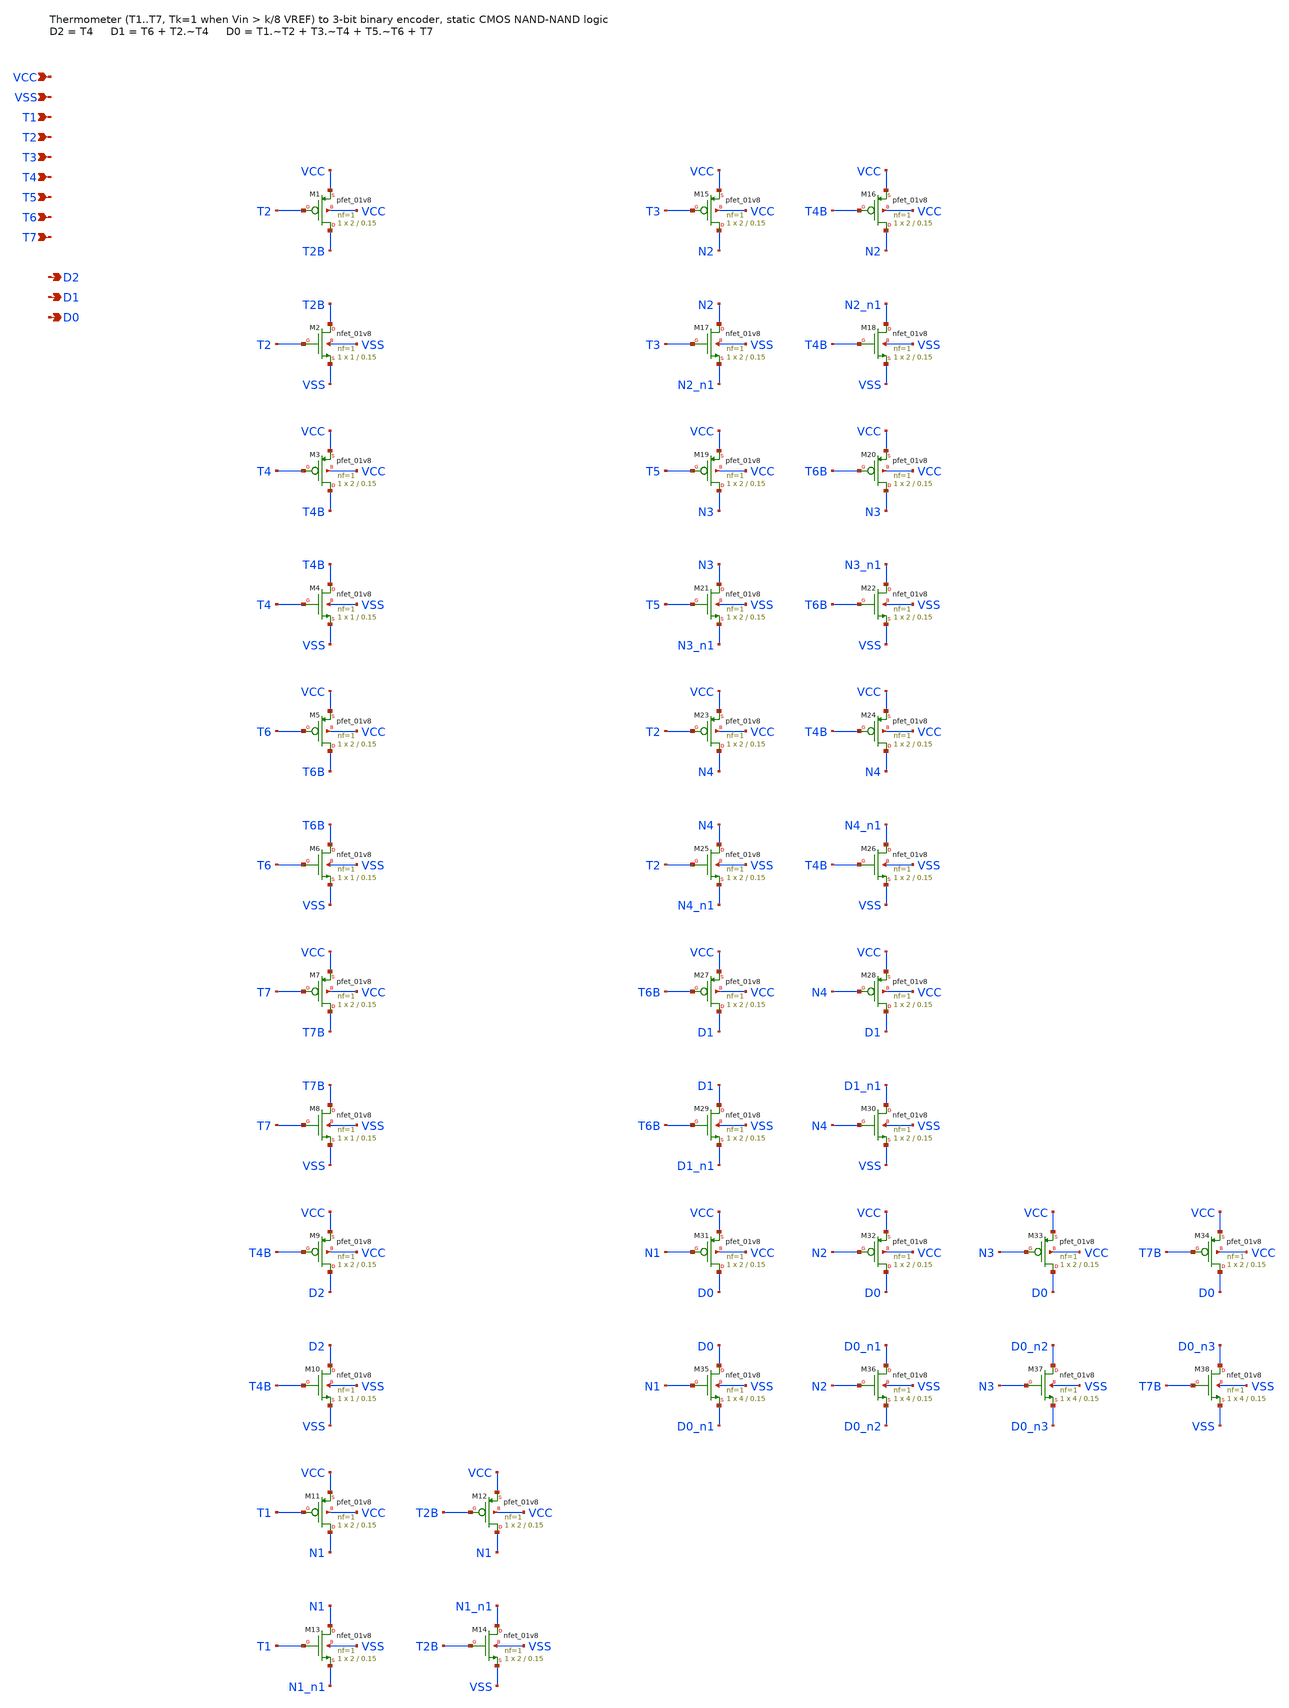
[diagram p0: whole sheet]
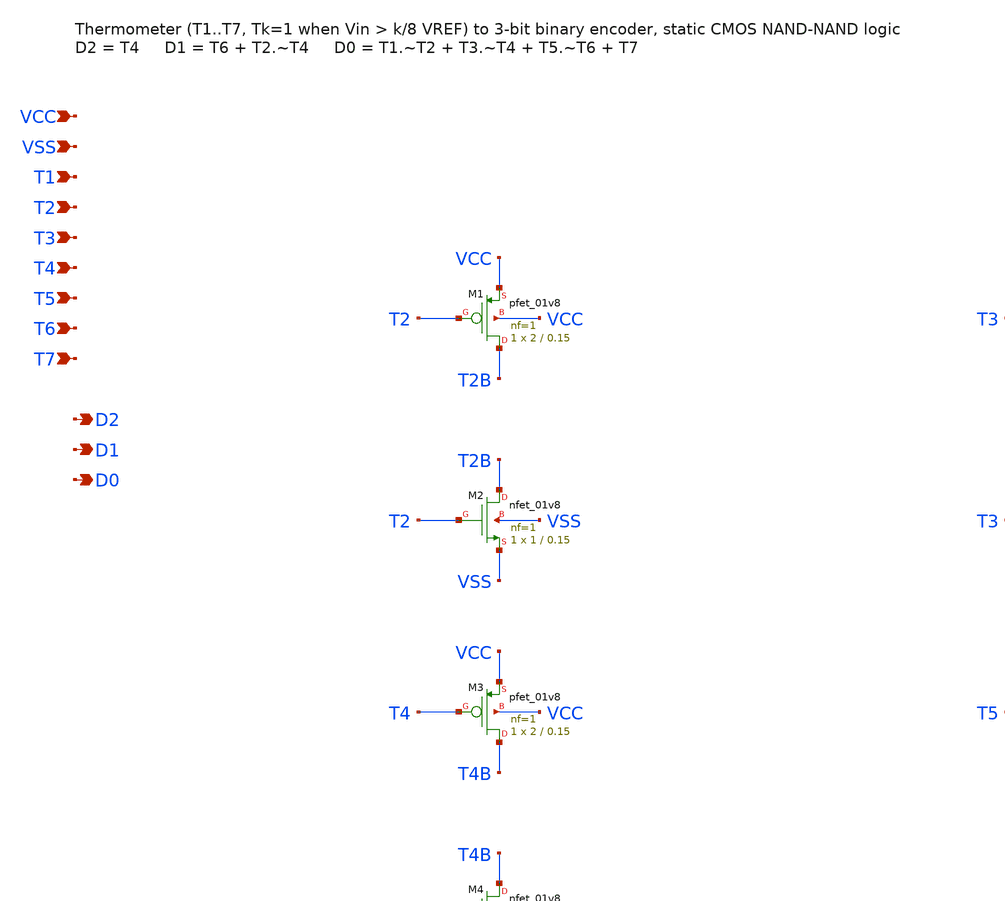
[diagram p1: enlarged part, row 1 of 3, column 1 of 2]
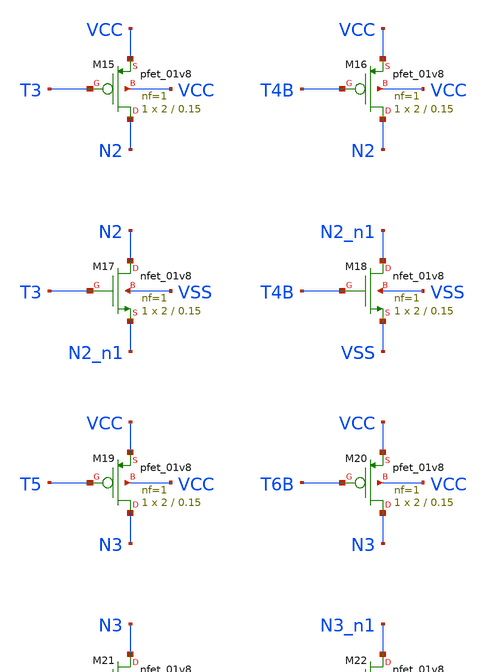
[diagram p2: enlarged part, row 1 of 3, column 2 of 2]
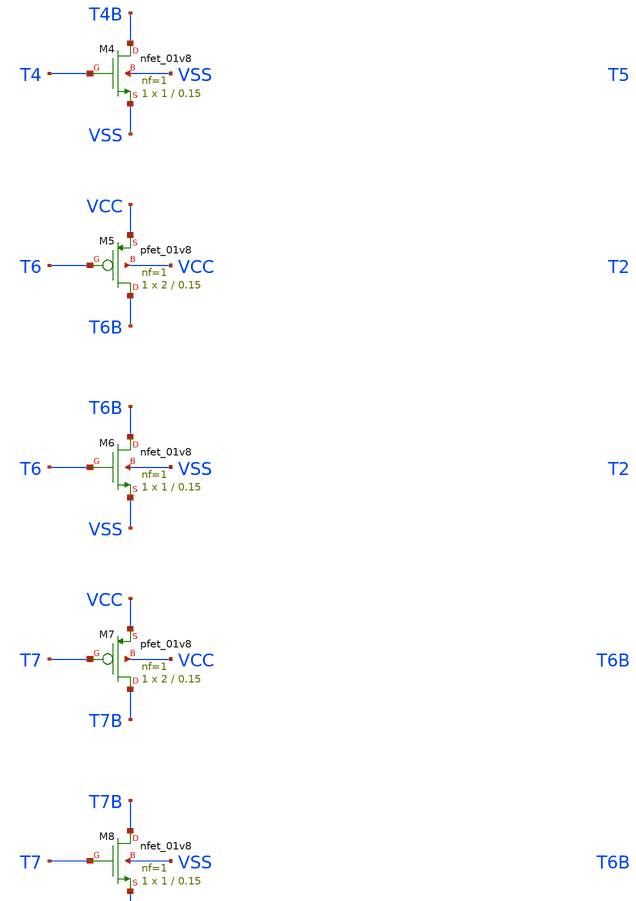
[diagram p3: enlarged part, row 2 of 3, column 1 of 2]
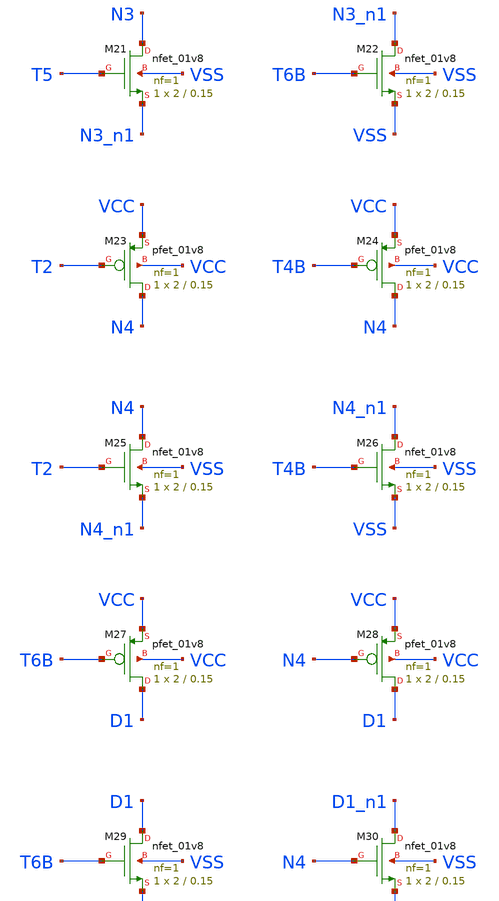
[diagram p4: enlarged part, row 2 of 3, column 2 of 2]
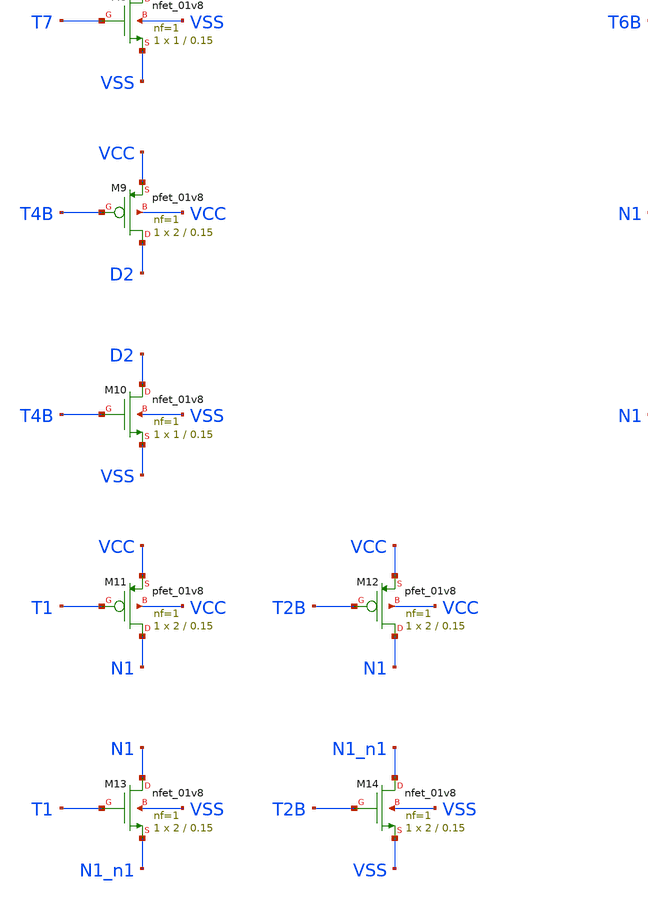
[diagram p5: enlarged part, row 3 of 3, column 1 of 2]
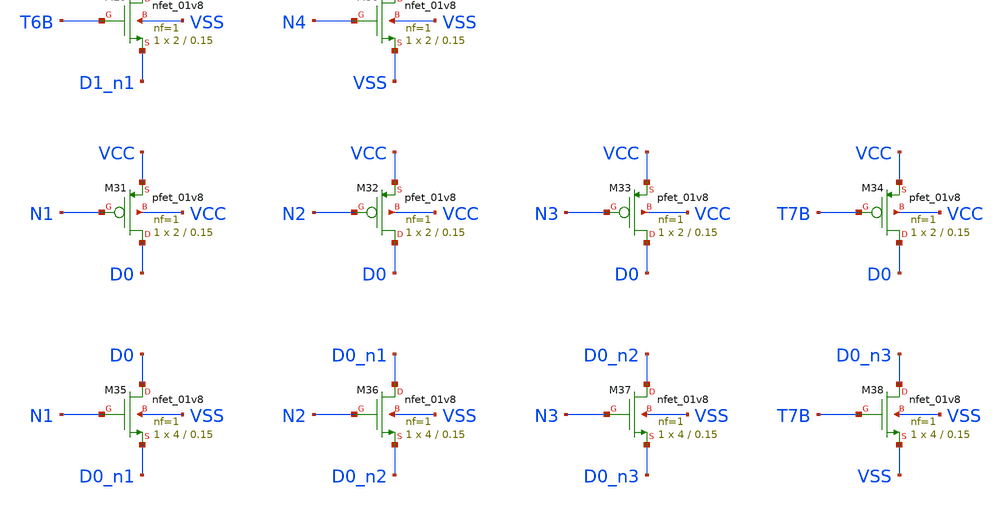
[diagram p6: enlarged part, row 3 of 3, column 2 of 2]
** sch_path: therm2bin3.sch
**.subckt therm2bin3 VCC VSS T1 T2 T3 T4 T5 T6 T7 D2 D1 D0
*.ipin VCC
*.ipin VSS
*.ipin T1
*.ipin T2
*.ipin T3
*.ipin T4
*.ipin T5
*.ipin T6
*.ipin T7
*.opin D2
*.opin D1
*.opin D0
XM1 T2B T2 VCC VCC sky130_fd_pr__pfet_01v8 L=0.15 W=2 nf=1 ad='int((nf+1)/2) * W/nf * 0.29' as='int((nf+2)/2) * W/nf * 0.29'
+ pd='2*int((nf+1)/2) * (W/nf + 0.29)' ps='2*int((nf+2)/2) * (W/nf + 0.29)' nrd='0.29 / W' nrs='0.29 / W'
+ sa=0 sb=0 sd=0 mult=1 m=1
XM2 T2B T2 VSS VSS sky130_fd_pr__nfet_01v8 L=0.15 W=1 nf=1 ad='int((nf+1)/2) * W/nf * 0.29' as='int((nf+2)/2) * W/nf * 0.29'
+ pd='2*int((nf+1)/2) * (W/nf + 0.29)' ps='2*int((nf+2)/2) * (W/nf + 0.29)' nrd='0.29 / W' nrs='0.29 / W'
+ sa=0 sb=0 sd=0 mult=1 m=1
XM3 T4B T4 VCC VCC sky130_fd_pr__pfet_01v8 L=0.15 W=2 nf=1 ad='int((nf+1)/2) * W/nf * 0.29' as='int((nf+2)/2) * W/nf * 0.29'
+ pd='2*int((nf+1)/2) * (W/nf + 0.29)' ps='2*int((nf+2)/2) * (W/nf + 0.29)' nrd='0.29 / W' nrs='0.29 / W'
+ sa=0 sb=0 sd=0 mult=1 m=1
XM4 T4B T4 VSS VSS sky130_fd_pr__nfet_01v8 L=0.15 W=1 nf=1 ad='int((nf+1)/2) * W/nf * 0.29' as='int((nf+2)/2) * W/nf * 0.29'
+ pd='2*int((nf+1)/2) * (W/nf + 0.29)' ps='2*int((nf+2)/2) * (W/nf + 0.29)' nrd='0.29 / W' nrs='0.29 / W'
+ sa=0 sb=0 sd=0 mult=1 m=1
XM5 T6B T6 VCC VCC sky130_fd_pr__pfet_01v8 L=0.15 W=2 nf=1 ad='int((nf+1)/2) * W/nf * 0.29' as='int((nf+2)/2) * W/nf * 0.29'
+ pd='2*int((nf+1)/2) * (W/nf + 0.29)' ps='2*int((nf+2)/2) * (W/nf + 0.29)' nrd='0.29 / W' nrs='0.29 / W'
+ sa=0 sb=0 sd=0 mult=1 m=1
XM6 T6B T6 VSS VSS sky130_fd_pr__nfet_01v8 L=0.15 W=1 nf=1 ad='int((nf+1)/2) * W/nf * 0.29' as='int((nf+2)/2) * W/nf * 0.29'
+ pd='2*int((nf+1)/2) * (W/nf + 0.29)' ps='2*int((nf+2)/2) * (W/nf + 0.29)' nrd='0.29 / W' nrs='0.29 / W'
+ sa=0 sb=0 sd=0 mult=1 m=1
XM7 T7B T7 VCC VCC sky130_fd_pr__pfet_01v8 L=0.15 W=2 nf=1 ad='int((nf+1)/2) * W/nf * 0.29' as='int((nf+2)/2) * W/nf * 0.29'
+ pd='2*int((nf+1)/2) * (W/nf + 0.29)' ps='2*int((nf+2)/2) * (W/nf + 0.29)' nrd='0.29 / W' nrs='0.29 / W'
+ sa=0 sb=0 sd=0 mult=1 m=1
XM8 T7B T7 VSS VSS sky130_fd_pr__nfet_01v8 L=0.15 W=1 nf=1 ad='int((nf+1)/2) * W/nf * 0.29' as='int((nf+2)/2) * W/nf * 0.29'
+ pd='2*int((nf+1)/2) * (W/nf + 0.29)' ps='2*int((nf+2)/2) * (W/nf + 0.29)' nrd='0.29 / W' nrs='0.29 / W'
+ sa=0 sb=0 sd=0 mult=1 m=1
XM9 D2 T4B VCC VCC sky130_fd_pr__pfet_01v8 L=0.15 W=2 nf=1 ad='int((nf+1)/2) * W/nf * 0.29' as='int((nf+2)/2) * W/nf * 0.29'
+ pd='2*int((nf+1)/2) * (W/nf + 0.29)' ps='2*int((nf+2)/2) * (W/nf + 0.29)' nrd='0.29 / W' nrs='0.29 / W'
+ sa=0 sb=0 sd=0 mult=1 m=1
XM10 D2 T4B VSS VSS sky130_fd_pr__nfet_01v8 L=0.15 W=1 nf=1 ad='int((nf+1)/2) * W/nf * 0.29' as='int((nf+2)/2) * W/nf * 0.29'
+ pd='2*int((nf+1)/2) * (W/nf + 0.29)' ps='2*int((nf+2)/2) * (W/nf + 0.29)' nrd='0.29 / W' nrs='0.29 / W'
+ sa=0 sb=0 sd=0 mult=1 m=1
XM11 N1 T1 VCC VCC sky130_fd_pr__pfet_01v8 L=0.15 W=2 nf=1 ad='int((nf+1)/2) * W/nf * 0.29' as='int((nf+2)/2) * W/nf * 0.29'
+ pd='2*int((nf+1)/2) * (W/nf + 0.29)' ps='2*int((nf+2)/2) * (W/nf + 0.29)' nrd='0.29 / W' nrs='0.29 / W'
+ sa=0 sb=0 sd=0 mult=1 m=1
XM12 N1 T2B VCC VCC sky130_fd_pr__pfet_01v8 L=0.15 W=2 nf=1 ad='int((nf+1)/2) * W/nf * 0.29' as='int((nf+2)/2) * W/nf * 0.29'
+ pd='2*int((nf+1)/2) * (W/nf + 0.29)' ps='2*int((nf+2)/2) * (W/nf + 0.29)' nrd='0.29 / W' nrs='0.29 / W'
+ sa=0 sb=0 sd=0 mult=1 m=1
XM13 N1 T1 N1_n1 VSS sky130_fd_pr__nfet_01v8 L=0.15 W=2 nf=1 ad='int((nf+1)/2) * W/nf * 0.29' as='int((nf+2)/2) * W/nf * 0.29'
+ pd='2*int((nf+1)/2) * (W/nf + 0.29)' ps='2*int((nf+2)/2) * (W/nf + 0.29)' nrd='0.29 / W' nrs='0.29 / W'
+ sa=0 sb=0 sd=0 mult=1 m=1
XM14 N1_n1 T2B VSS VSS sky130_fd_pr__nfet_01v8 L=0.15 W=2 nf=1 ad='int((nf+1)/2) * W/nf * 0.29' as='int((nf+2)/2) * W/nf * 0.29'
+ pd='2*int((nf+1)/2) * (W/nf + 0.29)' ps='2*int((nf+2)/2) * (W/nf + 0.29)' nrd='0.29 / W' nrs='0.29 / W'
+ sa=0 sb=0 sd=0 mult=1 m=1
XM15 N2 T3 VCC VCC sky130_fd_pr__pfet_01v8 L=0.15 W=2 nf=1 ad='int((nf+1)/2) * W/nf * 0.29' as='int((nf+2)/2) * W/nf * 0.29'
+ pd='2*int((nf+1)/2) * (W/nf + 0.29)' ps='2*int((nf+2)/2) * (W/nf + 0.29)' nrd='0.29 / W' nrs='0.29 / W'
+ sa=0 sb=0 sd=0 mult=1 m=1
XM16 N2 T4B VCC VCC sky130_fd_pr__pfet_01v8 L=0.15 W=2 nf=1 ad='int((nf+1)/2) * W/nf * 0.29' as='int((nf+2)/2) * W/nf * 0.29'
+ pd='2*int((nf+1)/2) * (W/nf + 0.29)' ps='2*int((nf+2)/2) * (W/nf + 0.29)' nrd='0.29 / W' nrs='0.29 / W'
+ sa=0 sb=0 sd=0 mult=1 m=1
XM17 N2 T3 N2_n1 VSS sky130_fd_pr__nfet_01v8 L=0.15 W=2 nf=1 ad='int((nf+1)/2) * W/nf * 0.29' as='int((nf+2)/2) * W/nf * 0.29'
+ pd='2*int((nf+1)/2) * (W/nf + 0.29)' ps='2*int((nf+2)/2) * (W/nf + 0.29)' nrd='0.29 / W' nrs='0.29 / W'
+ sa=0 sb=0 sd=0 mult=1 m=1
XM18 N2_n1 T4B VSS VSS sky130_fd_pr__nfet_01v8 L=0.15 W=2 nf=1 ad='int((nf+1)/2) * W/nf * 0.29' as='int((nf+2)/2) * W/nf * 0.29'
+ pd='2*int((nf+1)/2) * (W/nf + 0.29)' ps='2*int((nf+2)/2) * (W/nf + 0.29)' nrd='0.29 / W' nrs='0.29 / W'
+ sa=0 sb=0 sd=0 mult=1 m=1
XM19 N3 T5 VCC VCC sky130_fd_pr__pfet_01v8 L=0.15 W=2 nf=1 ad='int((nf+1)/2) * W/nf * 0.29' as='int((nf+2)/2) * W/nf * 0.29'
+ pd='2*int((nf+1)/2) * (W/nf + 0.29)' ps='2*int((nf+2)/2) * (W/nf + 0.29)' nrd='0.29 / W' nrs='0.29 / W'
+ sa=0 sb=0 sd=0 mult=1 m=1
XM20 N3 T6B VCC VCC sky130_fd_pr__pfet_01v8 L=0.15 W=2 nf=1 ad='int((nf+1)/2) * W/nf * 0.29' as='int((nf+2)/2) * W/nf * 0.29'
+ pd='2*int((nf+1)/2) * (W/nf + 0.29)' ps='2*int((nf+2)/2) * (W/nf + 0.29)' nrd='0.29 / W' nrs='0.29 / W'
+ sa=0 sb=0 sd=0 mult=1 m=1
XM21 N3 T5 N3_n1 VSS sky130_fd_pr__nfet_01v8 L=0.15 W=2 nf=1 ad='int((nf+1)/2) * W/nf * 0.29' as='int((nf+2)/2) * W/nf * 0.29'
+ pd='2*int((nf+1)/2) * (W/nf + 0.29)' ps='2*int((nf+2)/2) * (W/nf + 0.29)' nrd='0.29 / W' nrs='0.29 / W'
+ sa=0 sb=0 sd=0 mult=1 m=1
XM22 N3_n1 T6B VSS VSS sky130_fd_pr__nfet_01v8 L=0.15 W=2 nf=1 ad='int((nf+1)/2) * W/nf * 0.29' as='int((nf+2)/2) * W/nf * 0.29'
+ pd='2*int((nf+1)/2) * (W/nf + 0.29)' ps='2*int((nf+2)/2) * (W/nf + 0.29)' nrd='0.29 / W' nrs='0.29 / W'
+ sa=0 sb=0 sd=0 mult=1 m=1
XM23 N4 T2 VCC VCC sky130_fd_pr__pfet_01v8 L=0.15 W=2 nf=1 ad='int((nf+1)/2) * W/nf * 0.29' as='int((nf+2)/2) * W/nf * 0.29'
+ pd='2*int((nf+1)/2) * (W/nf + 0.29)' ps='2*int((nf+2)/2) * (W/nf + 0.29)' nrd='0.29 / W' nrs='0.29 / W'
+ sa=0 sb=0 sd=0 mult=1 m=1
XM24 N4 T4B VCC VCC sky130_fd_pr__pfet_01v8 L=0.15 W=2 nf=1 ad='int((nf+1)/2) * W/nf * 0.29' as='int((nf+2)/2) * W/nf * 0.29'
+ pd='2*int((nf+1)/2) * (W/nf + 0.29)' ps='2*int((nf+2)/2) * (W/nf + 0.29)' nrd='0.29 / W' nrs='0.29 / W'
+ sa=0 sb=0 sd=0 mult=1 m=1
XM25 N4 T2 N4_n1 VSS sky130_fd_pr__nfet_01v8 L=0.15 W=2 nf=1 ad='int((nf+1)/2) * W/nf * 0.29' as='int((nf+2)/2) * W/nf * 0.29'
+ pd='2*int((nf+1)/2) * (W/nf + 0.29)' ps='2*int((nf+2)/2) * (W/nf + 0.29)' nrd='0.29 / W' nrs='0.29 / W'
+ sa=0 sb=0 sd=0 mult=1 m=1
XM26 N4_n1 T4B VSS VSS sky130_fd_pr__nfet_01v8 L=0.15 W=2 nf=1 ad='int((nf+1)/2) * W/nf * 0.29' as='int((nf+2)/2) * W/nf * 0.29'
+ pd='2*int((nf+1)/2) * (W/nf + 0.29)' ps='2*int((nf+2)/2) * (W/nf + 0.29)' nrd='0.29 / W' nrs='0.29 / W'
+ sa=0 sb=0 sd=0 mult=1 m=1
XM27 D1 T6B VCC VCC sky130_fd_pr__pfet_01v8 L=0.15 W=2 nf=1 ad='int((nf+1)/2) * W/nf * 0.29' as='int((nf+2)/2) * W/nf * 0.29'
+ pd='2*int((nf+1)/2) * (W/nf + 0.29)' ps='2*int((nf+2)/2) * (W/nf + 0.29)' nrd='0.29 / W' nrs='0.29 / W'
+ sa=0 sb=0 sd=0 mult=1 m=1
XM28 D1 N4 VCC VCC sky130_fd_pr__pfet_01v8 L=0.15 W=2 nf=1 ad='int((nf+1)/2) * W/nf * 0.29' as='int((nf+2)/2) * W/nf * 0.29'
+ pd='2*int((nf+1)/2) * (W/nf + 0.29)' ps='2*int((nf+2)/2) * (W/nf + 0.29)' nrd='0.29 / W' nrs='0.29 / W'
+ sa=0 sb=0 sd=0 mult=1 m=1
XM29 D1 T6B D1_n1 VSS sky130_fd_pr__nfet_01v8 L=0.15 W=2 nf=1 ad='int((nf+1)/2) * W/nf * 0.29' as='int((nf+2)/2) * W/nf * 0.29'
+ pd='2*int((nf+1)/2) * (W/nf + 0.29)' ps='2*int((nf+2)/2) * (W/nf + 0.29)' nrd='0.29 / W' nrs='0.29 / W'
+ sa=0 sb=0 sd=0 mult=1 m=1
XM30 D1_n1 N4 VSS VSS sky130_fd_pr__nfet_01v8 L=0.15 W=2 nf=1 ad='int((nf+1)/2) * W/nf * 0.29' as='int((nf+2)/2) * W/nf * 0.29'
+ pd='2*int((nf+1)/2) * (W/nf + 0.29)' ps='2*int((nf+2)/2) * (W/nf + 0.29)' nrd='0.29 / W' nrs='0.29 / W'
+ sa=0 sb=0 sd=0 mult=1 m=1
XM31 D0 N1 VCC VCC sky130_fd_pr__pfet_01v8 L=0.15 W=2 nf=1 ad='int((nf+1)/2) * W/nf * 0.29' as='int((nf+2)/2) * W/nf * 0.29'
+ pd='2*int((nf+1)/2) * (W/nf + 0.29)' ps='2*int((nf+2)/2) * (W/nf + 0.29)' nrd='0.29 / W' nrs='0.29 / W'
+ sa=0 sb=0 sd=0 mult=1 m=1
XM32 D0 N2 VCC VCC sky130_fd_pr__pfet_01v8 L=0.15 W=2 nf=1 ad='int((nf+1)/2) * W/nf * 0.29' as='int((nf+2)/2) * W/nf * 0.29'
+ pd='2*int((nf+1)/2) * (W/nf + 0.29)' ps='2*int((nf+2)/2) * (W/nf + 0.29)' nrd='0.29 / W' nrs='0.29 / W'
+ sa=0 sb=0 sd=0 mult=1 m=1
XM33 D0 N3 VCC VCC sky130_fd_pr__pfet_01v8 L=0.15 W=2 nf=1 ad='int((nf+1)/2) * W/nf * 0.29' as='int((nf+2)/2) * W/nf * 0.29'
+ pd='2*int((nf+1)/2) * (W/nf + 0.29)' ps='2*int((nf+2)/2) * (W/nf + 0.29)' nrd='0.29 / W' nrs='0.29 / W'
+ sa=0 sb=0 sd=0 mult=1 m=1
XM34 D0 T7B VCC VCC sky130_fd_pr__pfet_01v8 L=0.15 W=2 nf=1 ad='int((nf+1)/2) * W/nf * 0.29' as='int((nf+2)/2) * W/nf * 0.29'
+ pd='2*int((nf+1)/2) * (W/nf + 0.29)' ps='2*int((nf+2)/2) * (W/nf + 0.29)' nrd='0.29 / W' nrs='0.29 / W'
+ sa=0 sb=0 sd=0 mult=1 m=1
XM35 D0 N1 D0_n1 VSS sky130_fd_pr__nfet_01v8 L=0.15 W=4 nf=1 ad='int((nf+1)/2) * W/nf * 0.29' as='int((nf+2)/2) * W/nf * 0.29'
+ pd='2*int((nf+1)/2) * (W/nf + 0.29)' ps='2*int((nf+2)/2) * (W/nf + 0.29)' nrd='0.29 / W' nrs='0.29 / W'
+ sa=0 sb=0 sd=0 mult=1 m=1
XM36 D0_n1 N2 D0_n2 VSS sky130_fd_pr__nfet_01v8 L=0.15 W=4 nf=1 ad='int((nf+1)/2) * W/nf * 0.29' as='int((nf+2)/2) * W/nf * 0.29'
+ pd='2*int((nf+1)/2) * (W/nf + 0.29)' ps='2*int((nf+2)/2) * (W/nf + 0.29)' nrd='0.29 / W' nrs='0.29 / W'
+ sa=0 sb=0 sd=0 mult=1 m=1
XM37 D0_n2 N3 D0_n3 VSS sky130_fd_pr__nfet_01v8 L=0.15 W=4 nf=1 ad='int((nf+1)/2) * W/nf * 0.29' as='int((nf+2)/2) * W/nf * 0.29'
+ pd='2*int((nf+1)/2) * (W/nf + 0.29)' ps='2*int((nf+2)/2) * (W/nf + 0.29)' nrd='0.29 / W' nrs='0.29 / W'
+ sa=0 sb=0 sd=0 mult=1 m=1
XM38 D0_n3 T7B VSS VSS sky130_fd_pr__nfet_01v8 L=0.15 W=4 nf=1 ad='int((nf+1)/2) * W/nf * 0.29' as='int((nf+2)/2) * W/nf * 0.29'
+ pd='2*int((nf+1)/2) * (W/nf + 0.29)' ps='2*int((nf+2)/2) * (W/nf + 0.29)' nrd='0.29 / W' nrs='0.29 / W'
+ sa=0 sb=0 sd=0 mult=1 m=1
**.ends
.end
